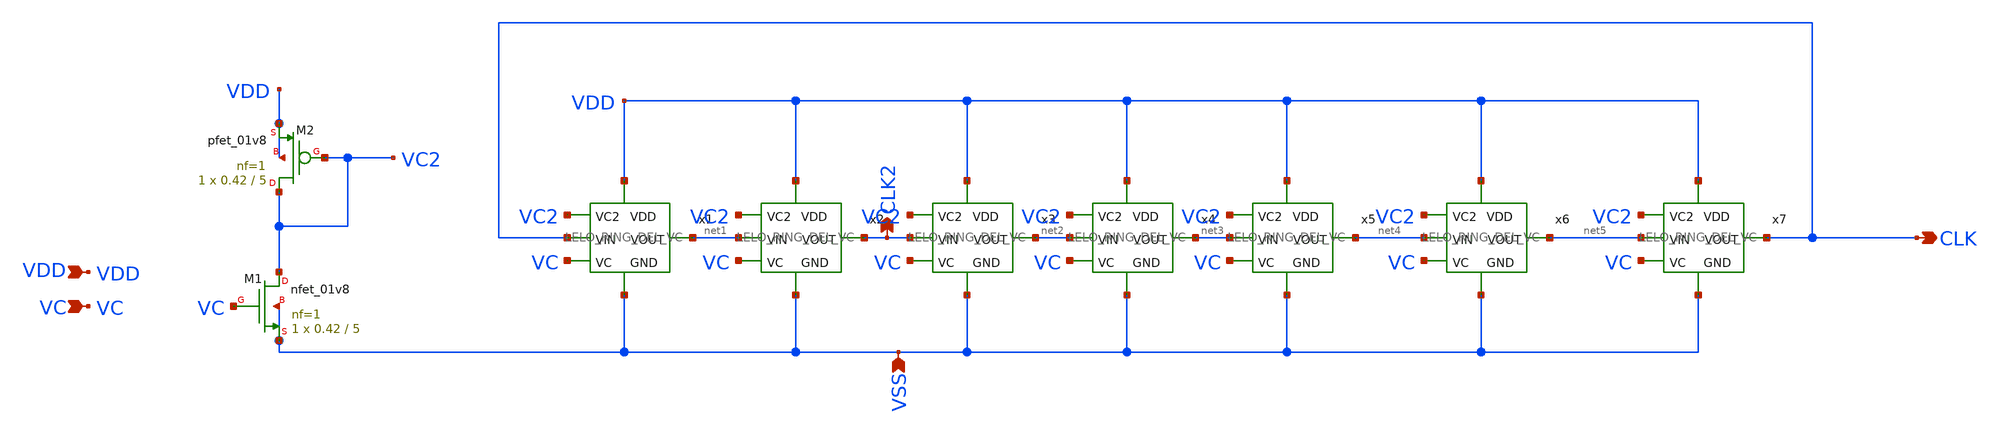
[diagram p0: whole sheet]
** sch_path: design/LELO_SVOD_SKY130A/RO.sch
**.subckt RO CLK VSS CLK2 VDD VC
*.opin CLK
*.ipin VSS
*.opin CLK2
*.ipin VDD
*.ipin VC
x1 VDD VC2 CLK net1 VC VSS LELO_RING_DEL_VC
x2 VDD VC2 net1 CLK2 VC VSS LELO_RING_DEL_VC
x3 VDD VC2 CLK2 net2 VC VSS LELO_RING_DEL_VC
x4 VDD VC2 net2 net3 VC VSS LELO_RING_DEL_VC
x5 VDD VC2 net3 net4 VC VSS LELO_RING_DEL_VC
x6 VDD VC2 net4 net5 VC VSS LELO_RING_DEL_VC
x7 VDD VC2 net5 CLK VC VSS LELO_RING_DEL_VC
XM1 VC2 VC VSS VSS sky130_fd_pr__nfet_01v8 L=5 W=0.42 nf=1 ad='int((1 + 1)/2) * 0.42 / 1 * 0.29' as='int((1 + 2)/2) * 0.42 / 1 * 0.29'
+ pd='2*int((1 + 1)/2) * (0.42 / 1 + 0.29)' ps='2*int((1 + 2)/2) * (0.42 / 1 + 0.29)' nrd='0.29 / 0.42 '
+ nrs='0.29 / 0.42 ' sa=0 sb=0 sd=0 mult=1 m=1
XM2 VC2 VC2 VDD VDD sky130_fd_pr__pfet_01v8 L=5 W=0.42 nf=1 ad='int((1 + 1)/2) * 0.42 / 1 * 0.29' as='int((1 + 2)/2) * 0.42 / 1 * 0.29'
+ pd='2*int((1 + 1)/2) * (0.42 / 1 + 0.29)' ps='2*int((1 + 2)/2) * (0.42 / 1 + 0.29)' nrd='0.29 / 0.42 '
+ nrs='0.29 / 0.42 ' sa=0 sb=0 sd=0 mult=1 m=1
**.ends

* expanding   symbol:  LELO_SVOD_SKY130A/LELO_RING_DEL_VC.sym # of pins=6
** sym_path: design/LELO_SVOD_SKY130A/LELO_RING_DEL_VC.sym
** sch_path: design/LELO_SVOD_SKY130A/LELO_RING_DEL_VC.sch
.subckt LELO_RING_DEL_VC VDD VC2 VIN VOUT VC GND
*.ipin VIN
*.ipin VDD
*.ipin GND
*.opin VOUT
*.ipin VC
*.ipin VC2
XM1 net2 VC2 VDD VDD sky130_fd_pr__pfet_01v8 L=5 W=0.42 nf=1 ad='int((1 + 1)/2) * 0.42 / 1 * 0.29' as='int((1 + 2)/2) * 0.42 / 1 * 0.29'
+ pd='2*int((1 + 1)/2) * (0.42 / 1 + 0.29)' ps='2*int((1 + 2)/2) * (0.42 / 1 + 0.29)' nrd='0.29 / 0.42 '
+ nrs='0.29 / 0.42 ' sa=0 sb=0 sd=0 mult=1 m=1
XM2 VOUT VIN net2 net2 sky130_fd_pr__pfet_01v8 L=5 W=0.42 nf=1 ad='int((1 + 1)/2) * 0.42 / 1 * 0.29'
+ as='int((1 + 2)/2) * 0.42 / 1 * 0.29' pd='2*int((1 + 1)/2) * (0.42 / 1 + 0.29)' ps='2*int((1 + 2)/2) * (0.42 / 1 + 0.29)'
+ nrd='0.29 / 0.42 ' nrs='0.29 / 0.42 ' sa=0 sb=0 sd=0 mult=1 m=1
XM3 VOUT VIN net1 GND sky130_fd_pr__nfet_01v8 L=5 W=0.42 nf=1 ad='int((1 + 1)/2) * 0.42 / 1 * 0.29' as='int((1 + 2)/2) * 0.42 / 1 * 0.29'
+ pd='2*int((1 + 1)/2) * (0.42 / 1 + 0.29)' ps='2*int((1 + 2)/2) * (0.42 / 1 + 0.29)' nrd='0.29 / 0.42 '
+ nrs='0.29 / 0.42 ' sa=0 sb=0 sd=0 mult=1 m=1
XM4 net1 VC GND GND sky130_fd_pr__nfet_01v8 L=5 W=0.42 nf=1 ad='int((1 + 1)/2) * 0.42 / 1 * 0.29' as='int((1 + 2)/2) * 0.42 / 1 * 0.29'
+ pd='2*int((1 + 1)/2) * (0.42 / 1 + 0.29)' ps='2*int((1 + 2)/2) * (0.42 / 1 + 0.29)' nrd='0.29 / 0.42 '
+ nrs='0.29 / 0.42 ' sa=0 sb=0 sd=0 mult=1 m=1
.ends

.end
